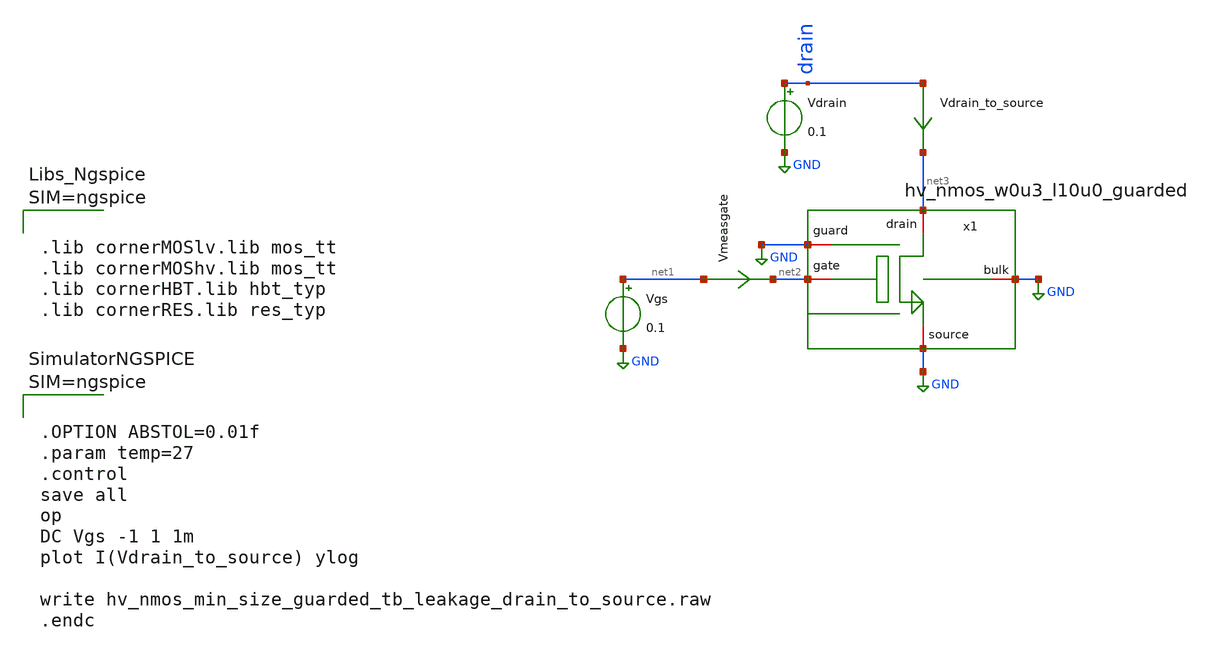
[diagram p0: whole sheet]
** sch_path: trident_test_structures/design_data/xschem/transistor_characterization/hv_nmos_w0u3_l10u0_guarded/hv_nmos_w0u3_l10u0_guarded_tb_leakage_drain_to_source.sch
**.subckt hv_nmos_w0u3_l10u0_guarded_tb_leakage_drain_to_source
Vdrain drain GND 0.1
Vdrain_to_source drain net3 0
.save i(vdrain_to_source)
Vgs net1 GND 0.1
Vmeasgate net1 net2 0
.save i(vmeasgate)
x1 net3 GND net2 GND GND hv_nmos_w0u3_l10u0_guarded
**** begin user architecture code



.lib cornerMOSlv.lib mos_tt
.lib cornerMOShv.lib mos_tt
.lib cornerHBT.lib hbt_typ
.lib cornerRES.lib res_typ






.OPTION ABSTOL=0.01f
.param temp=27
.control
save all
op
DC Vgs -1 1 1m
plot I(Vdrain_to_source) ylog

write hv_nmos_min_size_guarded_tb_leakage_drain_to_source.raw
.endc



**** end user architecture code
**.ends

* expanding   symbol:  hv_nmos_w0u3_l10u0_guarded.sym # of pins=5
** sym_path: trident_test_structures/design_data/xschem/transistor_characterization/hv_nmos_w0u3_l10u0_guarded/hv_nmos_w0u3_l10u0_guarded.sym
** sch_path: trident_test_structures/design_data/xschem/transistor_characterization/hv_nmos_w0u3_l10u0_guarded/hv_nmos_w0u3_l10u0_guarded.sch
.subckt hv_nmos_w0u3_l10u0_guarded drain guard gate bulk source
*.iopin gate
*.iopin drain
*.iopin source
*.iopin bulk
*.iopin guard
XM1 drain gate source sub! sg13_hv_nmos w=0.3u l=10u ng=1 m=1 mm_ok=1
XR1 bulk sub! ptap1 R=32.37 w=10.33e-6 l=0.78e-6
.ends

.GLOBAL GND
.GLOBAL sub!
.end
